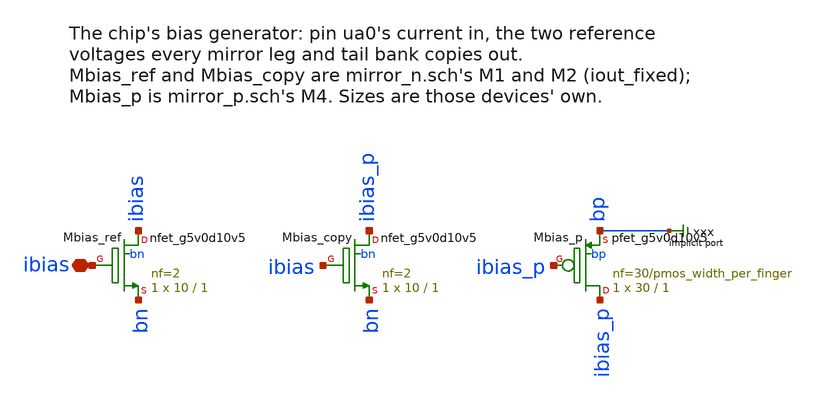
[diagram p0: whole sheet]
** sch_path: xschem/mosbius_lib/mosbius_bias.sch
**.subckt mosbius_bias ibias
*.iopin ibias
XMbias_ref ibias ibias bn bn sky130_fd_pr__nfet_g5v0d10v5 L=1 W=10 nf=2 ad='int((nf+1)/2) * W/nf * 0.29'
+ as='int((nf+2)/2) * W/nf * 0.29' pd='2*int((nf+1)/2) * (W/nf + 0.29)' ps='2*int((nf+2)/2) * (W/nf + 0.29)'
+ nrd='0.29 / W' nrs='0.29 / W' sa=0 sb=0 sd=0 mult=1 m=1
XMbias_copy ibias_p ibias bn bn sky130_fd_pr__nfet_g5v0d10v5 L=1 W=10 nf=2 ad='int((nf+1)/2) * W/nf * 0.29'
+ as='int((nf+2)/2) * W/nf * 0.29' pd='2*int((nf+1)/2) * (W/nf + 0.29)' ps='2*int((nf+2)/2) * (W/nf + 0.29)'
+ nrd='0.29 / W' nrs='0.29 / W' sa=0 sb=0 sd=0 mult=1 m=1
XMbias_p ibias_p ibias_p bp bp sky130_fd_pr__pfet_g5v0d10v5 L=1 W=30 nf=30/pmos_width_per_finger ad='int((nf+1)/2) * W/nf * 0.29'
+ as='int((nf+2)/2) * W/nf * 0.29' pd='2*int((nf+1)/2) * (W/nf + 0.29)' ps='2*int((nf+2)/2) * (W/nf + 0.29)'
+ nrd='0.29 / W' nrs='0.29 / W' sa=0 sb=0 sd=0 mult=1 m=1
* implicit port xxx
**.ends
.end
